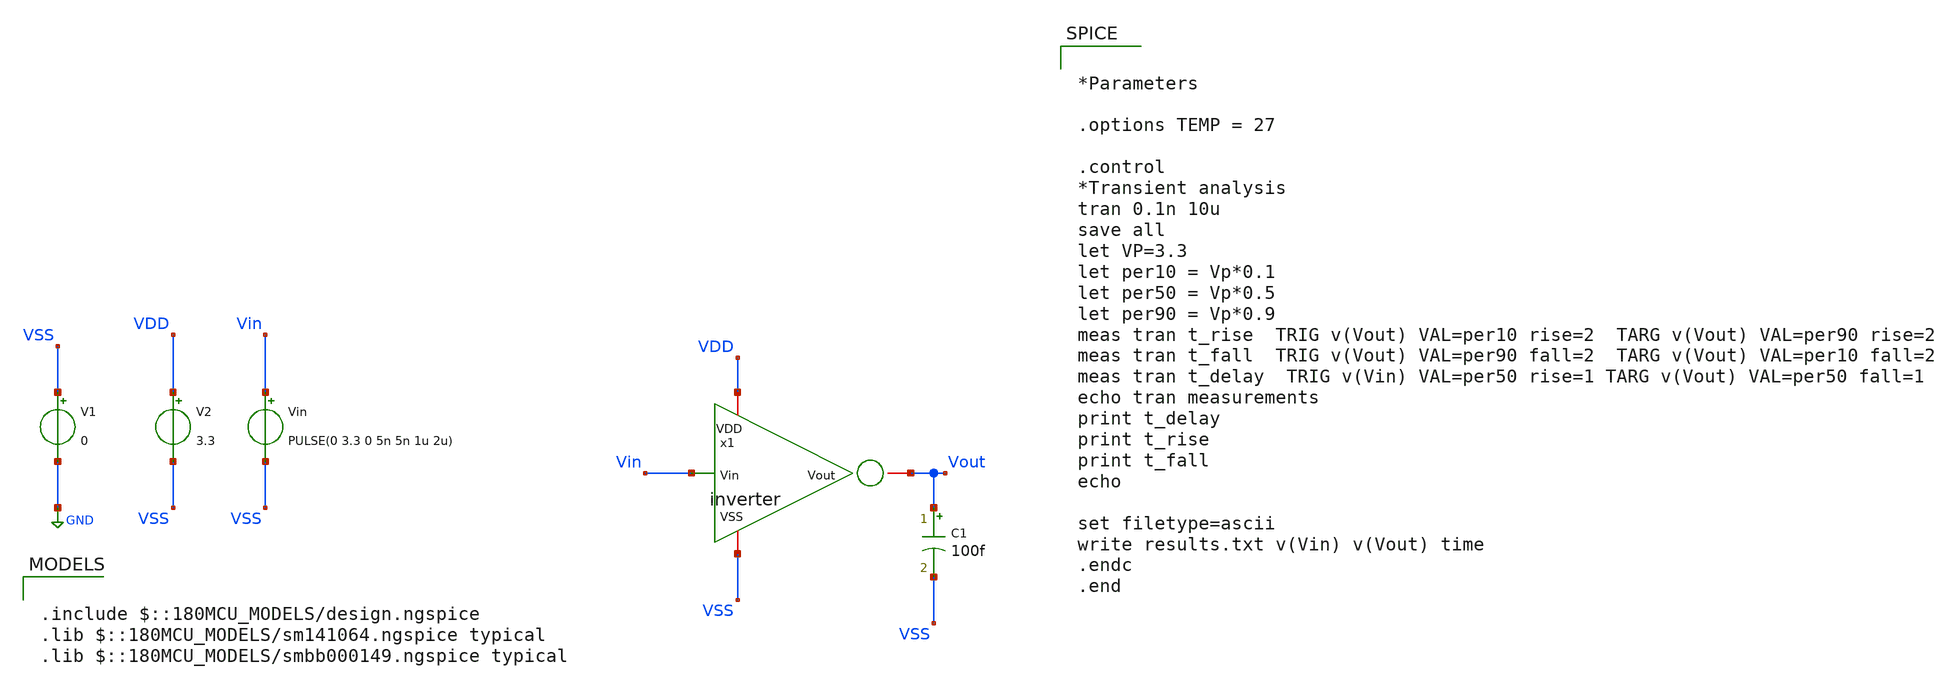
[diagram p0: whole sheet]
** sch_path: Modulo_Analogico/Laboratorios/Lab2/inv_tb.sch
**.subckt inv_tb
x1 Vin VDD VSS Vout inverter
C1 Vout VSS 100f m=1
V1 VSS GND 0
V2 VDD VSS 3.3
Vin Vin VSS PULSE(0 3.3 0 5n 5n 1u 2u)
**** begin user architecture code

.include $::180MCU_MODELS/design.ngspice
.lib $::180MCU_MODELS/sm141064.ngspice typical
.lib $::180MCU_MODELS/smbb000149.ngspice typical



*Parameters

.options TEMP = 27

.control
*Transient analysis
tran 0.1n 10u
save all
let VP=3.3
let per10 = Vp*0.1
let per50 = Vp*0.5
let per90 = Vp*0.9
meas tran t_rise  TRIG v(Vout) VAL=per10 rise=2  TARG v(Vout) VAL=per90 rise=2
meas tran t_fall  TRIG v(Vout) VAL=per90 fall=2  TARG v(Vout) VAL=per10 fall=2
meas tran t_delay  TRIG v(Vin) VAL=per50 rise=1 TARG v(Vout) VAL=per50 fall=1
echo tran measurements
print t_delay
print t_rise
print t_fall
echo

set filetype=ascii
write results.txt v(Vin) v(Vout) time
.endc
.end


**** end user architecture code
**.ends
.GLOBAL GND
.end
